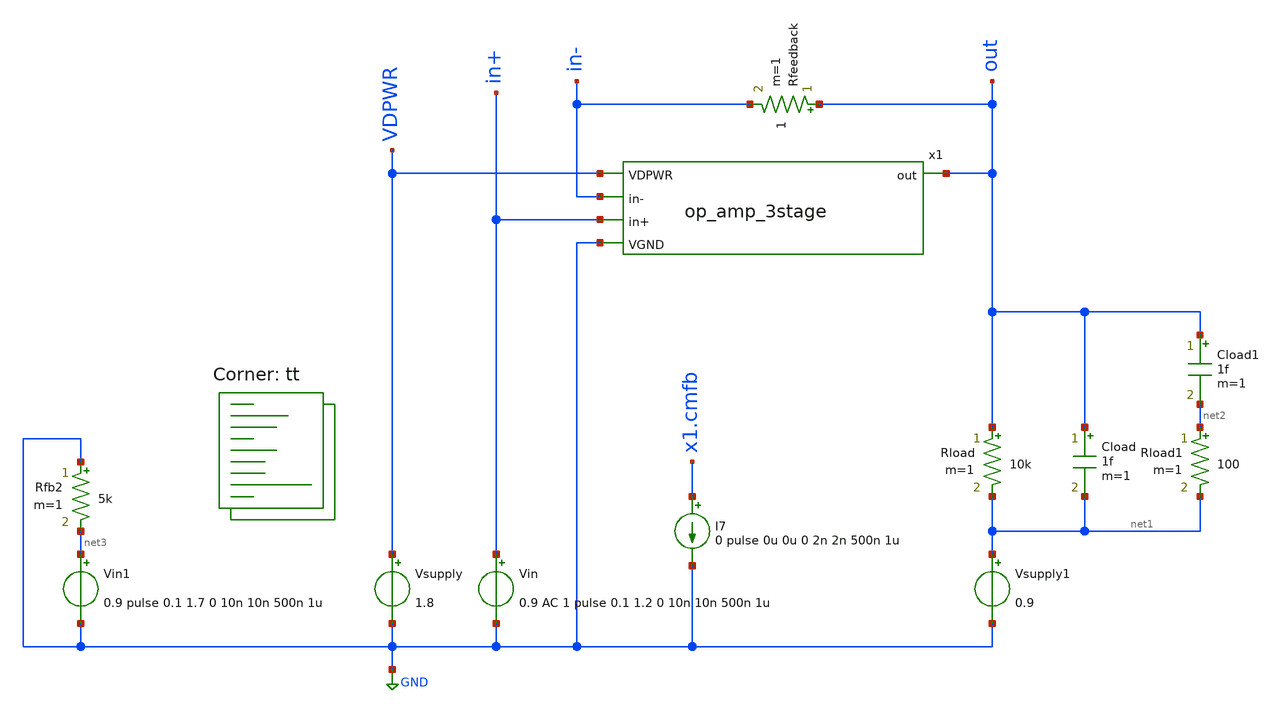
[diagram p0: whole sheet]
** sch_path: xschem/tb_op_amp_3stage.sch
**.subckt tb_op_amp_3stage
Vin in+ GND 0.9 AC 1 pulse 0.1 1.2 0 10n 10n 500n 1u
Vsupply VDPWR GND 1.8
Rload out net1 10k m=1
Vsupply1 net1 GND 0.9
Rload1 net2 net1 100 m=1
Cload out net1 1f m=1
Cload1 out net2 1f m=1
I7 x1.cmfb GND 0 pulse 0u 0u 0 2n 2n 500n 1u
x1 VDPWR out in- in+ GND op_amp_3stage
Rfeedback out in- 1 m=1
Vin1 net3 GND 0.9 pulse 0.1 1.7 0 10n 10n 500n 1u
Rfb2 GND net3 5k m=1
**** begin user architecture code
.lib $::SKYWATER_MODELS/sky130.lib.spice tt


.control
.option savecurrents
*.options temp=125
dc Vin 0.1 1.2 0.02
*temp -40 125 15
plot v(in+) v(x1.commonmode) v(VDPWR)
plot v(out) v(x1.pdrive) v(x1.ndrive)
plot v(in+)-v(in-) ylimit 100u -100u ydelta 50u
plot @m.x1.xm2.msky130_fd_pr__pfet_01v8_lvt[id] @m.x1.xm1.msky130_fd_pr__nfet_01v8_lvt[id]
plot 1/(@m.x1.xm2.msky130_fd_pr__pfet_01v8_lvt[gm]+@m.x1.xm1.msky130_fd_pr__nfet_01v8_lvt[gm])
*plot i(Vmeas) title vs_Supply_tt_-40degto125deg
ac dec 100 1 1e9
plot db(v(out)/v(in+,in-)) ph(v(out)/v(in+,in-))*57.3 ylimit 180 -180 ydelta 20
plot db(v(out)/v(x1.in+2,x1.in-2)) ph(v(out)/v(x1.in+2,x1.in-2))*57.3 ylimit 180 -180 ydelta 20
plot db(v(out)) xlog ylimit 6 -6 ydelta 3
dc temp -40 125 5
*plot v(out) v(pdrive) v(ndrive)
*plot i(Vmeas) title vs_Temp_tt
*plot v(x1.drive) title vs_Temp_tt
*plot v(x1.ptat) title vs_Temp_tt
*set temp=-40
*tran 2n 1u
*plot v(VSS) title Start_Up_tt_-40deg
*plot v(x1.ptat) title Stability
*plot i(Vmeas) @m.x1.xm18.msky130_fd_pr__nfet_01v8[id] title Start_Up_tt
*set temp=125
tran 2n 1u
plot v(out) v(x1.pdrive) v(x1.ndrive)
plot @m.x1.xm2.msky130_fd_pr__pfet_01v8_lvt[id]
*plot v(out) ylimit 0.86 1.04 ydelta 0.02
plot v(out)
plot v(x1.cmfb)
*plot V(VSS) title Start_Up_tt_125deg
*plot v(x1.ptat)
*plot i(Vmeas) @m.x1.xm18.msky130_fd_pr__nfet_01v8[id] title Start_Up_tt_125deg
noise v(out) Vin dec 10 1 100MEG 1
write noise1.all noise2.all
setplot noise1
setplot noise2
plot onoise_spectrum xlog ylog
*plot onoise.m.x1.xm15.msky130_fd_pr__pfet_01v8_lvt onoise.m.x1.xm14.msky130_fd_pr__nfet_01v8_lvt
*+ xlog ylog
*plot onoise.m.x1.xm14.msky130_fd_pr__nfet_01v8_lvt onoise.m.x1.xm14.msky130_fd_pr__nfet_01v8_lvt.id
*+ xlog ylog
save all
*set temp=27
op
print all
write tb_op_amp_3stage.raw
.endc
.save all @m.x1.xm1.msky130_fd_pr__nfet_01v8_lvt[gm] @m.x1.xm2.msky130_fd_pr__pfet_01v8_lvt[gm]  @m.x1.xm11.msky130_fd_pr__pfet_01v8[gm] @m.x1.xm12.msky130_fd_pr__pfet_01v8[gm]  @m.x1.xm15.msky130_fd_pr__pfet_01v8_lvt[gm] @m.x1.xm16.msky130_fd_pr__pfet_01v8_lvt[gm]  @m.x1.xm14.msky130_fd_pr__nfet_01v8_lvt[gm] @m.x1.xm13.msky130_fd_pr__nfet_01v8_lvt[gm]


**** end user architecture code
**.ends

* expanding   symbol:  /foss/designs/tt09-analog-opamp-3stage/xschem/op_amp_3stage.sym # of pins=5
** sym_path: xschem/op_amp_3stage.sym
** sch_path: xschem/op_amp_3stage.sch
.subckt op_amp_3stage VDPWR out in- in+ VGND
*.opin out
*.ipin VDPWR
*.ipin VGND
*.ipin in-
*.ipin in+
XM2 out pdrive VDPWR VDPWR sky130_fd_pr__pfet_01v8_lvt L=0.35 W=110 nf=11 ad='int((nf+1)/2) * W/nf * 0.29'
+ as='int((nf+2)/2) * W/nf * 0.29' pd='2*int((nf+1)/2) * (W/nf + 0.29)' ps='2*int((nf+2)/2) * (W/nf + 0.29)'
+ nrd='0.29 / W' nrs='0.29 / W' sa=0 sb=0 sd=0 mult=2 m=2
XM6 net2 net2 VDPWR VDPWR sky130_fd_pr__pfet_01v8_lvt L=0.35 W=10.0 nf=1 ad='int((nf+1)/2) * W/nf * 0.29'
+ as='int((nf+2)/2) * W/nf * 0.29' pd='2*int((nf+1)/2) * (W/nf + 0.29)' ps='2*int((nf+2)/2) * (W/nf + 0.29)'
+ nrd='0.29 / W' nrs='0.29 / W' sa=0 sb=0 sd=0 mult=1 m=1
XM8 ndrive I2_10uA<-- pdrive VDPWR sky130_fd_pr__pfet_01v8_lvt L=0.35 W=10.0 nf=1 ad='int((nf+1)/2) * W/nf * 0.29'
+ as='int((nf+2)/2) * W/nf * 0.29' pd='2*int((nf+1)/2) * (W/nf + 0.29)' ps='2*int((nf+2)/2) * (W/nf + 0.29)'
+ nrd='0.29 / W' nrs='0.29 / W' sa=0 sb=0 sd=0 mult=1 m=1
XM7 I2_10uA<-- I2_10uA<-- net2 VDPWR sky130_fd_pr__pfet_01v8_lvt L=0.35 W=10.0 nf=1 ad='int((nf+1)/2) * W/nf * 0.29'
+ as='int((nf+2)/2) * W/nf * 0.29' pd='2*int((nf+1)/2) * (W/nf + 0.29)' ps='2*int((nf+2)/2) * (W/nf + 0.29)'
+ nrd='0.29 / W' nrs='0.29 / W' sa=0 sb=0 sd=0 mult=1 m=1
XM3 <--I3_10uA <--I3_10uA net1 VGND sky130_fd_pr__nfet_01v8_lvt L=0.35 W=2.5 nf=1 ad='int((nf+1)/2) * W/nf * 0.29'
+ as='int((nf+2)/2) * W/nf * 0.29' pd='2*int((nf+1)/2) * (W/nf + 0.29)' ps='2*int((nf+2)/2) * (W/nf + 0.29)'
+ nrd='0.29 / W' nrs='0.29 / W' sa=0 sb=0 sd=0 mult=1 m=1
M5 pdrive <--I3_10uA ndrive VGND sky130_fd_pr__nfet_01v8_lvt L=0.35 W=2.5 nf=1 ad='int((nf+1)/2) * W/nf * 0.29'
+ as='int((nf+2)/2) * W/nf * 0.29' pd='2*int((nf+1)/2) * (W/nf + 0.29)' ps='2*int((nf+2)/2) * (W/nf + 0.29)'
+ nrd='0.29 / W' nrs='0.29 / W' sa=0 sb=0 sd=0 mult=1 m=1
XM4 net1 net1 VGND VGND sky130_fd_pr__nfet_01v8_lvt L=0.35 W=2.5 nf=1 ad='int((nf+1)/2) * W/nf * 0.29'
+ as='int((nf+2)/2) * W/nf * 0.29' pd='2*int((nf+1)/2) * (W/nf + 0.29)' ps='2*int((nf+2)/2) * (W/nf + 0.29)'
+ nrd='0.29 / W' nrs='0.29 / W' sa=0 sb=0 sd=0 mult=1 m=1
XM1 out ndrive VGND VGND sky130_fd_pr__nfet_01v8_lvt L=0.35 W=42.5 nf=17 ad='int((nf+1)/2) * W/nf * 0.29'
+ as='int((nf+2)/2) * W/nf * 0.29' pd='2*int((nf+1)/2) * (W/nf + 0.29)' ps='2*int((nf+2)/2) * (W/nf + 0.29)'
+ nrd='0.29 / W' nrs='0.29 / W' sa=0 sb=0 sd=0 mult=2 m=2
XM9 ndrive net3 VGND VGND sky130_fd_pr__nfet_01v8_lvt L=1.0 W=2.0 nf=1 ad='int((nf+1)/2) * W/nf * 0.29'
+ as='int((nf+2)/2) * W/nf * 0.29' pd='2*int((nf+1)/2) * (W/nf + 0.29)' ps='2*int((nf+2)/2) * (W/nf + 0.29)'
+ nrd='0.29 / W' nrs='0.29 / W' sa=0 sb=0 sd=0 mult=1 m=1
XM10 net3 net3 VGND VGND sky130_fd_pr__nfet_01v8_lvt L=1.0 W=2.0 nf=1 ad='int((nf+1)/2) * W/nf * 0.29'
+ as='int((nf+2)/2) * W/nf * 0.29' pd='2*int((nf+1)/2) * (W/nf + 0.29)' ps='2*int((nf+2)/2) * (W/nf + 0.29)'
+ nrd='0.29 / W' nrs='0.29 / W' sa=0 sb=0 sd=0 mult=1 m=1
XM11 net3 in-2 <--I4_20uA VDPWR sky130_fd_pr__pfet_01v8 L=0.7 W=20 nf=2 ad='int((nf+1)/2) * W/nf * 0.29'
+ as='int((nf+2)/2) * W/nf * 0.29' pd='2*int((nf+1)/2) * (W/nf + 0.29)' ps='2*int((nf+2)/2) * (W/nf + 0.29)'
+ nrd='0.29 / W' nrs='0.29 / W' sa=0 sb=0 sd=0 mult=1 m=1
XM12 ndrive in+2 <--I4_20uA VDPWR sky130_fd_pr__pfet_01v8 L=0.7 W=20 nf=2 ad='int((nf+1)/2) * W/nf * 0.29'
+ as='int((nf+2)/2) * W/nf * 0.29' pd='2*int((nf+1)/2) * (W/nf + 0.29)' ps='2*int((nf+2)/2) * (W/nf + 0.29)'
+ nrd='0.29 / W' nrs='0.29 / W' sa=0 sb=0 sd=0 mult=1 m=1
XC1 out ndrive sky130_fd_pr__cap_mim_m3_1 W=27 L=10 MF=1 m=1
XC2 out pdrive sky130_fd_pr__cap_mim_m3_1 W=27 L=10 MF=1 m=1
XM13 in-2 net4 VGND VGND sky130_fd_pr__nfet_01v8_lvt L=8 W=40 nf=2 ad='int((nf+1)/2) * W/nf * 0.29' as='int((nf+2)/2) * W/nf * 0.29'
+ pd='2*int((nf+1)/2) * (W/nf + 0.29)' ps='2*int((nf+2)/2) * (W/nf + 0.29)' nrd='0.29 / W' nrs='0.29 / W'
+ sa=0 sb=0 sd=0 mult=1 m=1
XM14 in+2 net4 VGND VGND sky130_fd_pr__nfet_01v8_lvt L=8 W=40 nf=2 ad='int((nf+1)/2) * W/nf * 0.29' as='int((nf+2)/2) * W/nf * 0.29'
+ pd='2*int((nf+1)/2) * (W/nf + 0.29)' ps='2*int((nf+2)/2) * (W/nf + 0.29)' nrd='0.29 / W' nrs='0.29 / W'
+ sa=0 sb=0 sd=0 mult=1 m=1
XC3 VGND in+2 sky130_fd_pr__cap_mim_m3_1 W=109 L=30 MF=1 m=1
XC4 out in-2 sky130_fd_pr__cap_mim_m3_1 W=109 L=30 MF=1 m=1
XM15 in+2 in- commonmode VDPWR sky130_fd_pr__pfet_01v8_lvt L=0.7 W=640 nf=32 ad='int((nf+1)/2) * W/nf * 0.29'
+ as='int((nf+2)/2) * W/nf * 0.29' pd='2*int((nf+1)/2) * (W/nf + 0.29)' ps='2*int((nf+2)/2) * (W/nf + 0.29)'
+ nrd='0.29 / W' nrs='0.29 / W' sa=0 sb=0 sd=0 mult=2 m=2
XM16 in-2 in+ commonmode VDPWR sky130_fd_pr__pfet_01v8_lvt L=0.7 W=640 nf=32 ad='int((nf+1)/2) * W/nf * 0.29'
+ as='int((nf+2)/2) * W/nf * 0.29' pd='2*int((nf+1)/2) * (W/nf + 0.29)' ps='2*int((nf+2)/2) * (W/nf + 0.29)'
+ nrd='0.29 / W' nrs='0.29 / W' sa=0 sb=0 sd=0 mult=2 m=2
XM19 net4 net4 VGND VGND sky130_fd_pr__nfet_01v8_lvt L=8 W=40 nf=2 ad='int((nf+1)/2) * W/nf * 0.29' as='int((nf+2)/2) * W/nf * 0.29'
+ pd='2*int((nf+1)/2) * (W/nf + 0.29)' ps='2*int((nf+2)/2) * (W/nf + 0.29)' nrd='0.29 / W' nrs='0.29 / W'
+ sa=0 sb=0 sd=0 mult=1 m=1
XM20 net4 VGND net5 VDPWR sky130_fd_pr__pfet_01v8 L=0.35 W=10 nf=1 ad='int((nf+1)/2) * W/nf * 0.29' as='int((nf+2)/2) * W/nf * 0.29'
+ pd='2*int((nf+1)/2) * (W/nf + 0.29)' ps='2*int((nf+2)/2) * (W/nf + 0.29)' nrd='0.29 / W' nrs='0.29 / W'
+ sa=0 sb=0 sd=0 mult=1 m=1
XM17 VGND in+2 cmfb VDPWR sky130_fd_pr__pfet_01v8 L=0.35 W=10 nf=1 ad='int((nf+1)/2) * W/nf * 0.29' as='int((nf+2)/2) * W/nf * 0.29'
+ pd='2*int((nf+1)/2) * (W/nf + 0.29)' ps='2*int((nf+2)/2) * (W/nf + 0.29)' nrd='0.29 / W' nrs='0.29 / W'
+ sa=0 sb=0 sd=0 mult=1 m=1
XM18 VGND in-2 cmfb VDPWR sky130_fd_pr__pfet_01v8 L=0.35 W=10 nf=1 ad='int((nf+1)/2) * W/nf * 0.29' as='int((nf+2)/2) * W/nf * 0.29'
+ pd='2*int((nf+1)/2) * (W/nf + 0.29)' ps='2*int((nf+2)/2) * (W/nf + 0.29)' nrd='0.29 / W' nrs='0.29 / W'
+ sa=0 sb=0 sd=0 mult=1 m=1
x1 VDPWR net6 VGND bias_generator
XM21 net6 net6 net7 VGND sky130_fd_pr__nfet_01v8_lvt L=4.0 W=3.0 nf=1 ad='int((nf+1)/2) * W/nf * 0.29'
+ as='int((nf+2)/2) * W/nf * 0.29' pd='2*int((nf+1)/2) * (W/nf + 0.29)' ps='2*int((nf+2)/2) * (W/nf + 0.29)'
+ nrd='0.29 / W' nrs='0.29 / W' sa=0 sb=0 sd=0 mult=1 m=1
XM23 net9 net6 net8 VGND sky130_fd_pr__nfet_01v8_lvt L=4.0 W=30 nf=10 ad='int((nf+1)/2) * W/nf * 0.29'
+ as='int((nf+2)/2) * W/nf * 0.29' pd='2*int((nf+1)/2) * (W/nf + 0.29)' ps='2*int((nf+2)/2) * (W/nf + 0.29)'
+ nrd='0.29 / W' nrs='0.29 / W' sa=0 sb=0 sd=0 mult=1 m=1
XM25 net10 net9 VDPWR VDPWR sky130_fd_pr__pfet_01v8 L=1.0 W=30 nf=3 ad='int((nf+1)/2) * W/nf * 0.29'
+ as='int((nf+2)/2) * W/nf * 0.29' pd='2*int((nf+1)/2) * (W/nf + 0.29)' ps='2*int((nf+2)/2) * (W/nf + 0.29)'
+ nrd='0.29 / W' nrs='0.29 / W' sa=0 sb=0 sd=0 mult=1 m=1
XM26 net11 net9 VDPWR VDPWR sky130_fd_pr__pfet_01v8 L=1.0 W=30 nf=3 ad='int((nf+1)/2) * W/nf * 0.29'
+ as='int((nf+2)/2) * W/nf * 0.29' pd='2*int((nf+1)/2) * (W/nf + 0.29)' ps='2*int((nf+2)/2) * (W/nf + 0.29)'
+ nrd='0.29 / W' nrs='0.29 / W' sa=0 sb=0 sd=0 mult=1 m=1
XM27 net12 net9 net10 VDPWR sky130_fd_pr__pfet_01v8_lvt L=0.35 W=10 nf=1 ad='int((nf+1)/2) * W/nf * 0.29'
+ as='int((nf+2)/2) * W/nf * 0.29' pd='2*int((nf+1)/2) * (W/nf + 0.29)' ps='2*int((nf+2)/2) * (W/nf + 0.29)'
+ nrd='0.29 / W' nrs='0.29 / W' sa=0 sb=0 sd=0 mult=1 m=1
XM28 net9 net9 net11 VDPWR sky130_fd_pr__pfet_01v8_lvt L=.35 W=10.0 nf=1 ad='int((nf+1)/2) * W/nf * 0.29'
+ as='int((nf+2)/2) * W/nf * 0.29' pd='2*int((nf+1)/2) * (W/nf + 0.29)' ps='2*int((nf+2)/2) * (W/nf + 0.29)'
+ nrd='0.29 / W' nrs='0.29 / W' sa=0 sb=0 sd=0 mult=1 m=1
XM22 net7 net7 VGND VGND sky130_fd_pr__nfet_01v8_lvt L=4.0 W=3.0 nf=1 ad='int((nf+1)/2) * W/nf * 0.29'
+ as='int((nf+2)/2) * W/nf * 0.29' pd='2*int((nf+1)/2) * (W/nf + 0.29)' ps='2*int((nf+2)/2) * (W/nf + 0.29)'
+ nrd='0.29 / W' nrs='0.29 / W' sa=0 sb=0 sd=0 mult=1 m=1
XM24 net8 net7 VGND VGND sky130_fd_pr__nfet_01v8_lvt L=4.0 W=3.0 nf=1 ad='int((nf+1)/2) * W/nf * 0.29'
+ as='int((nf+2)/2) * W/nf * 0.29' pd='2*int((nf+1)/2) * (W/nf + 0.29)' ps='2*int((nf+2)/2) * (W/nf + 0.29)'
+ nrd='0.29 / W' nrs='0.29 / W' sa=0 sb=0 sd=0 mult=10 m=10
XM29 net12 net12 net13 VGND sky130_fd_pr__nfet_01v8_lvt L=0.35 W=2.5 nf=1 ad='int((nf+1)/2) * W/nf * 0.29'
+ as='int((nf+2)/2) * W/nf * 0.29' pd='2*int((nf+1)/2) * (W/nf + 0.29)' ps='2*int((nf+2)/2) * (W/nf + 0.29)'
+ nrd='0.29 / W' nrs='0.29 / W' sa=0 sb=0 sd=0 mult=1 m=1
XM30 I2_10uA<-- net12 net14 VGND sky130_fd_pr__nfet_01v8_lvt L=0.35 W=2.5 nf=1 ad='int((nf+1)/2) * W/nf * 0.29'
+ as='int((nf+2)/2) * W/nf * 0.29' pd='2*int((nf+1)/2) * (W/nf + 0.29)' ps='2*int((nf+2)/2) * (W/nf + 0.29)'
+ nrd='0.29 / W' nrs='0.29 / W' sa=0 sb=0 sd=0 mult=1 m=1
XM31 net13 net13 VGND VGND sky130_fd_pr__nfet_01v8_lvt L=4.0 W=8.0 nf=1 ad='int((nf+1)/2) * W/nf * 0.29'
+ as='int((nf+2)/2) * W/nf * 0.29' pd='2*int((nf+1)/2) * (W/nf + 0.29)' ps='2*int((nf+2)/2) * (W/nf + 0.29)'
+ nrd='0.29 / W' nrs='0.29 / W' sa=0 sb=0 sd=0 mult=1 m=1
XM32 net14 net13 VGND VGND sky130_fd_pr__nfet_01v8_lvt L=4.0 W=8.0 nf=1 ad='int((nf+1)/2) * W/nf * 0.29'
+ as='int((nf+2)/2) * W/nf * 0.29' pd='2*int((nf+1)/2) * (W/nf + 0.29)' ps='2*int((nf+2)/2) * (W/nf + 0.29)'
+ nrd='0.29 / W' nrs='0.29 / W' sa=0 sb=0 sd=0 mult=1 m=1
XM34 ndrive net13 VGND VGND sky130_fd_pr__nfet_01v8_lvt L=4.0 W=8.0 nf=1 ad='int((nf+1)/2) * W/nf * 0.29'
+ as='int((nf+2)/2) * W/nf * 0.29' pd='2*int((nf+1)/2) * (W/nf + 0.29)' ps='2*int((nf+2)/2) * (W/nf + 0.29)'
+ nrd='0.29 / W' nrs='0.29 / W' sa=0 sb=0 sd=0 mult=2 m=2
XM33 net15 net9 VDPWR VDPWR sky130_fd_pr__pfet_01v8 L=1.0 W=30 nf=3 ad='int((nf+1)/2) * W/nf * 0.29'
+ as='int((nf+2)/2) * W/nf * 0.29' pd='2*int((nf+1)/2) * (W/nf + 0.29)' ps='2*int((nf+2)/2) * (W/nf + 0.29)'
+ nrd='0.29 / W' nrs='0.29 / W' sa=0 sb=0 sd=0 mult=1 m=1
XM35 <--I3_10uA net9 net15 VDPWR sky130_fd_pr__pfet_01v8_lvt L=0.35 W=10 nf=1 ad='int((nf+1)/2) * W/nf * 0.29'
+ as='int((nf+2)/2) * W/nf * 0.29' pd='2*int((nf+1)/2) * (W/nf + 0.29)' ps='2*int((nf+2)/2) * (W/nf + 0.29)'
+ nrd='0.29 / W' nrs='0.29 / W' sa=0 sb=0 sd=0 mult=1 m=1
XM36 net16 net9 VDPWR VDPWR sky130_fd_pr__pfet_01v8 L=1.0 W=30 nf=3 ad='int((nf+1)/2) * W/nf * 0.29'
+ as='int((nf+2)/2) * W/nf * 0.29' pd='2*int((nf+1)/2) * (W/nf + 0.29)' ps='2*int((nf+2)/2) * (W/nf + 0.29)'
+ nrd='0.29 / W' nrs='0.29 / W' sa=0 sb=0 sd=0 mult=2 m=2
XM37 pdrive net9 net16 VDPWR sky130_fd_pr__pfet_01v8_lvt L=0.35 W=10 nf=1 ad='int((nf+1)/2) * W/nf * 0.29'
+ as='int((nf+2)/2) * W/nf * 0.29' pd='2*int((nf+1)/2) * (W/nf + 0.29)' ps='2*int((nf+2)/2) * (W/nf + 0.29)'
+ nrd='0.29 / W' nrs='0.29 / W' sa=0 sb=0 sd=0 mult=2 m=2
XM38 net17 net9 VDPWR VDPWR sky130_fd_pr__pfet_01v8 L=1.0 W=30 nf=3 ad='int((nf+1)/2) * W/nf * 0.29'
+ as='int((nf+2)/2) * W/nf * 0.29' pd='2*int((nf+1)/2) * (W/nf + 0.29)' ps='2*int((nf+2)/2) * (W/nf + 0.29)'
+ nrd='0.29 / W' nrs='0.29 / W' sa=0 sb=0 sd=0 mult=2 m=2
XM39 <--I4_20uA net9 net17 VDPWR sky130_fd_pr__pfet_01v8_lvt L=0.35 W=10 nf=1 ad='int((nf+1)/2) * W/nf * 0.29'
+ as='int((nf+2)/2) * W/nf * 0.29' pd='2*int((nf+1)/2) * (W/nf + 0.29)' ps='2*int((nf+2)/2) * (W/nf + 0.29)'
+ nrd='0.29 / W' nrs='0.29 / W' sa=0 sb=0 sd=0 mult=2 m=2
XM40 net18 net9 VDPWR VDPWR sky130_fd_pr__pfet_01v8 L=1.0 W=30 nf=3 ad='int((nf+1)/2) * W/nf * 0.29'
+ as='int((nf+2)/2) * W/nf * 0.29' pd='2*int((nf+1)/2) * (W/nf + 0.29)' ps='2*int((nf+2)/2) * (W/nf + 0.29)'
+ nrd='0.29 / W' nrs='0.29 / W' sa=0 sb=0 sd=0 mult=4 m=4
XM41 commonmode net9 net18 VDPWR sky130_fd_pr__pfet_01v8_lvt L=0.35 W=10 nf=1 ad='int((nf+1)/2) * W/nf * 0.29'
+ as='int((nf+2)/2) * W/nf * 0.29' pd='2*int((nf+1)/2) * (W/nf + 0.29)' ps='2*int((nf+2)/2) * (W/nf + 0.29)'
+ nrd='0.29 / W' nrs='0.29 / W' sa=0 sb=0 sd=0 mult=4 m=4
XM42 net19 net9 VDPWR VDPWR sky130_fd_pr__pfet_01v8 L=1.0 W=30 nf=3 ad='int((nf+1)/2) * W/nf * 0.29'
+ as='int((nf+2)/2) * W/nf * 0.29' pd='2*int((nf+1)/2) * (W/nf + 0.29)' ps='2*int((nf+2)/2) * (W/nf + 0.29)'
+ nrd='0.29 / W' nrs='0.29 / W' sa=0 sb=0 sd=0 mult=4 m=4
XM43 cmfb net9 net19 VDPWR sky130_fd_pr__pfet_01v8_lvt L=0.35 W=10 nf=1 ad='int((nf+1)/2) * W/nf * 0.29'
+ as='int((nf+2)/2) * W/nf * 0.29' pd='2*int((nf+1)/2) * (W/nf + 0.29)' ps='2*int((nf+2)/2) * (W/nf + 0.29)'
+ nrd='0.29 / W' nrs='0.29 / W' sa=0 sb=0 sd=0 mult=4 m=4
XM44 net5 VGND cmfb VDPWR sky130_fd_pr__pfet_01v8 L=0.35 W=2.5 nf=1 ad='int((nf+1)/2) * W/nf * 0.29'
+ as='int((nf+2)/2) * W/nf * 0.29' pd='2*int((nf+1)/2) * (W/nf + 0.29)' ps='2*int((nf+2)/2) * (W/nf + 0.29)'
+ nrd='0.29 / W' nrs='0.29 / W' sa=0 sb=0 sd=0 mult=1 m=1
.ends


* expanding   symbol:  /foss/designs/tt09-analog-opamp-3stage/xschem/bias_generator.sym # of pins=3
** sym_path: xschem/bias_generator.sym
** sch_path: xschem/bias_generator.sch
.subckt bias_generator VDPWR i_out VGND
*.ipin VGND
*.ipin VDPWR
*.opin i_out
XM9 ncascode ncascode net1 VGND sky130_fd_pr__nfet_01v8_lvt L=1.0 W=8.0 nf=1 ad='int((nf+1)/2) * W/nf * 0.29'
+ as='int((nf+2)/2) * W/nf * 0.29' pd='2*int((nf+1)/2) * (W/nf + 0.29)' ps='2*int((nf+2)/2) * (W/nf + 0.29)'
+ nrd='0.29 / W' nrs='0.29 / W' sa=0 sb=0 sd=0 mult=1 m=1
XM10 pgate ncascode net4 VGND sky130_fd_pr__nfet_01v8_lvt L=1.0 W=8.0 nf=1 ad='int((nf+1)/2) * W/nf * 0.29'
+ as='int((nf+2)/2) * W/nf * 0.29' pd='2*int((nf+1)/2) * (W/nf + 0.29)' ps='2*int((nf+2)/2) * (W/nf + 0.29)'
+ nrd='0.29 / W' nrs='0.29 / W' sa=0 sb=0 sd=0 mult=1 m=1
XM2 net4 net1 ptat VGND sky130_fd_pr__nfet_01v8 L=1.0 W=8.0 nf=1 ad='int((nf+1)/2) * W/nf * 0.29' as='int((nf+2)/2) * W/nf * 0.29'
+ pd='2*int((nf+1)/2) * (W/nf + 0.29)' ps='2*int((nf+2)/2) * (W/nf + 0.29)' nrd='0.29 / W' nrs='0.29 / W'
+ sa=0 sb=0 sd=0 mult=8 m=8
XM18 pgate startup VGND VGND sky130_fd_pr__nfet_01v8 L=8.0 W=0.42 nf=1 ad='int((nf+1)/2) * W/nf * 0.29'
+ as='int((nf+2)/2) * W/nf * 0.29' pd='2*int((nf+1)/2) * (W/nf + 0.29)' ps='2*int((nf+2)/2) * (W/nf + 0.29)'
+ nrd='0.29 / W' nrs='0.29 / W' sa=0 sb=0 sd=0 mult=1 m=1
XM17 startup net1 VGND VGND sky130_fd_pr__nfet_01v8 L=1.0 W=8.0 nf=1 ad='int((nf+1)/2) * W/nf * 0.29'
+ as='int((nf+2)/2) * W/nf * 0.29' pd='2*int((nf+1)/2) * (W/nf + 0.29)' ps='2*int((nf+2)/2) * (W/nf + 0.29)'
+ nrd='0.29 / W' nrs='0.29 / W' sa=0 sb=0 sd=0 mult=1 m=1
XM1 net1 net1 VGND VGND sky130_fd_pr__nfet_01v8 L=1.0 W=8.0 nf=1 ad='int((nf+1)/2) * W/nf * 0.29' as='int((nf+2)/2) * W/nf * 0.29'
+ pd='2*int((nf+1)/2) * (W/nf + 0.29)' ps='2*int((nf+2)/2) * (W/nf + 0.29)' nrd='0.29 / W' nrs='0.29 / W'
+ sa=0 sb=0 sd=0 mult=1 m=1
XM5 ptat drive VGND VGND sky130_fd_pr__nfet_01v8 L=8.0 W=1.0 nf=1 ad='int((nf+1)/2) * W/nf * 0.29' as='int((nf+2)/2) * W/nf * 0.29'
+ pd='2*int((nf+1)/2) * (W/nf + 0.29)' ps='2*int((nf+2)/2) * (W/nf + 0.29)' nrd='0.29 / W' nrs='0.29 / W'
+ sa=0 sb=0 sd=0 mult=2 m=2
XM7 drive drive net3 VGND sky130_fd_pr__nfet_01v8 L=13.1 W=1.0 nf=1 ad='int((nf+1)/2) * W/nf * 0.29'
+ as='int((nf+2)/2) * W/nf * 0.29' pd='2*int((nf+1)/2) * (W/nf + 0.29)' ps='2*int((nf+2)/2) * (W/nf + 0.29)'
+ nrd='0.29 / W' nrs='0.29 / W' sa=0 sb=0 sd=0 mult=1 m=1
XM8 net3 drive ptat VGND sky130_fd_pr__nfet_01v8 L=8.0 W=1.0 nf=1 ad='int((nf+1)/2) * W/nf * 0.29' as='int((nf+2)/2) * W/nf * 0.29'
+ pd='2*int((nf+1)/2) * (W/nf + 0.29)' ps='2*int((nf+2)/2) * (W/nf + 0.29)' nrd='0.29 / W' nrs='0.29 / W'
+ sa=0 sb=0 sd=0 mult=1 m=1
XM4 net2 pgate VDPWR VDPWR sky130_fd_pr__pfet_01v8 L=1.0 W=8.0 nf=1 ad='int((nf+1)/2) * W/nf * 0.29'
+ as='int((nf+2)/2) * W/nf * 0.29' pd='2*int((nf+1)/2) * (W/nf + 0.29)' ps='2*int((nf+2)/2) * (W/nf + 0.29)'
+ nrd='0.29 / W' nrs='0.29 / W' sa=0 sb=0 sd=0 mult=1 m=1
XM6 net6 pgate VDPWR VDPWR sky130_fd_pr__pfet_01v8 L=1.0 W=8.0 nf=1 ad='int((nf+1)/2) * W/nf * 0.29'
+ as='int((nf+2)/2) * W/nf * 0.29' pd='2*int((nf+1)/2) * (W/nf + 0.29)' ps='2*int((nf+2)/2) * (W/nf + 0.29)'
+ nrd='0.29 / W' nrs='0.29 / W' sa=0 sb=0 sd=0 mult=1 m=1
XM14 net7 pgate VDPWR VDPWR sky130_fd_pr__pfet_01v8 L=1.0 W=8.0 nf=1 ad='int((nf+1)/2) * W/nf * 0.29'
+ as='int((nf+2)/2) * W/nf * 0.29' pd='2*int((nf+1)/2) * (W/nf + 0.29)' ps='2*int((nf+2)/2) * (W/nf + 0.29)'
+ nrd='0.29 / W' nrs='0.29 / W' sa=0 sb=0 sd=0 mult=1 m=1
XM3 net5 pgate VDPWR VDPWR sky130_fd_pr__pfet_01v8 L=1.0 W=8.0 nf=1 ad='int((nf+1)/2) * W/nf * 0.29'
+ as='int((nf+2)/2) * W/nf * 0.29' pd='2*int((nf+1)/2) * (W/nf + 0.29)' ps='2*int((nf+2)/2) * (W/nf + 0.29)'
+ nrd='0.29 / W' nrs='0.29 / W' sa=0 sb=0 sd=0 mult=1 m=1
XM16 startup net1 VDPWR VDPWR sky130_fd_pr__pfet_01v8 L=8.0 W=0.42 nf=1 ad='int((nf+1)/2) * W/nf * 0.29'
+ as='int((nf+2)/2) * W/nf * 0.29' pd='2*int((nf+1)/2) * (W/nf + 0.29)' ps='2*int((nf+2)/2) * (W/nf + 0.29)'
+ nrd='0.29 / W' nrs='0.29 / W' sa=0 sb=0 sd=0 mult=1 m=1
XM12 pgate pgate net2 VDPWR sky130_fd_pr__pfet_01v8_lvt L=1.0 W=8.0 nf=1 ad='int((nf+1)/2) * W/nf * 0.29'
+ as='int((nf+2)/2) * W/nf * 0.29' pd='2*int((nf+1)/2) * (W/nf + 0.29)' ps='2*int((nf+2)/2) * (W/nf + 0.29)'
+ nrd='0.29 / W' nrs='0.29 / W' sa=0 sb=0 sd=0 mult=1 m=1
XM13 drive pgate net6 VDPWR sky130_fd_pr__pfet_01v8_lvt L=1.0 W=8.0 nf=1 ad='int((nf+1)/2) * W/nf * 0.29'
+ as='int((nf+2)/2) * W/nf * 0.29' pd='2*int((nf+1)/2) * (W/nf + 0.29)' ps='2*int((nf+2)/2) * (W/nf + 0.29)'
+ nrd='0.29 / W' nrs='0.29 / W' sa=0 sb=0 sd=0 mult=1 m=1
XM15 i_out pgate net7 VDPWR sky130_fd_pr__pfet_01v8_lvt L=1.0 W=8.0 nf=1 ad='int((nf+1)/2) * W/nf * 0.29'
+ as='int((nf+2)/2) * W/nf * 0.29' pd='2*int((nf+1)/2) * (W/nf + 0.29)' ps='2*int((nf+2)/2) * (W/nf + 0.29)'
+ nrd='0.29 / W' nrs='0.29 / W' sa=0 sb=0 sd=0 mult=1 m=1
XM11 ncascode pgate net5 VDPWR sky130_fd_pr__pfet_01v8_lvt L=1.0 W=8.0 nf=1 ad='int((nf+1)/2) * W/nf * 0.29'
+ as='int((nf+2)/2) * W/nf * 0.29' pd='2*int((nf+1)/2) * (W/nf + 0.29)' ps='2*int((nf+2)/2) * (W/nf + 0.29)'
+ nrd='0.29 / W' nrs='0.29 / W' sa=0 sb=0 sd=0 mult=1 m=1
.ends

.GLOBAL GND
.end
